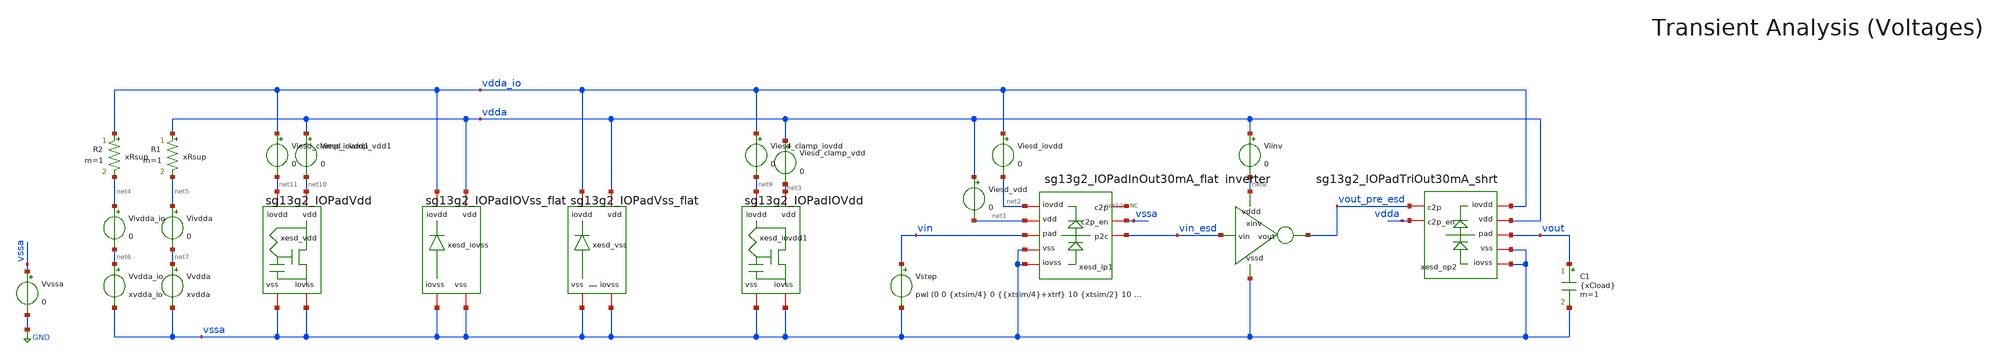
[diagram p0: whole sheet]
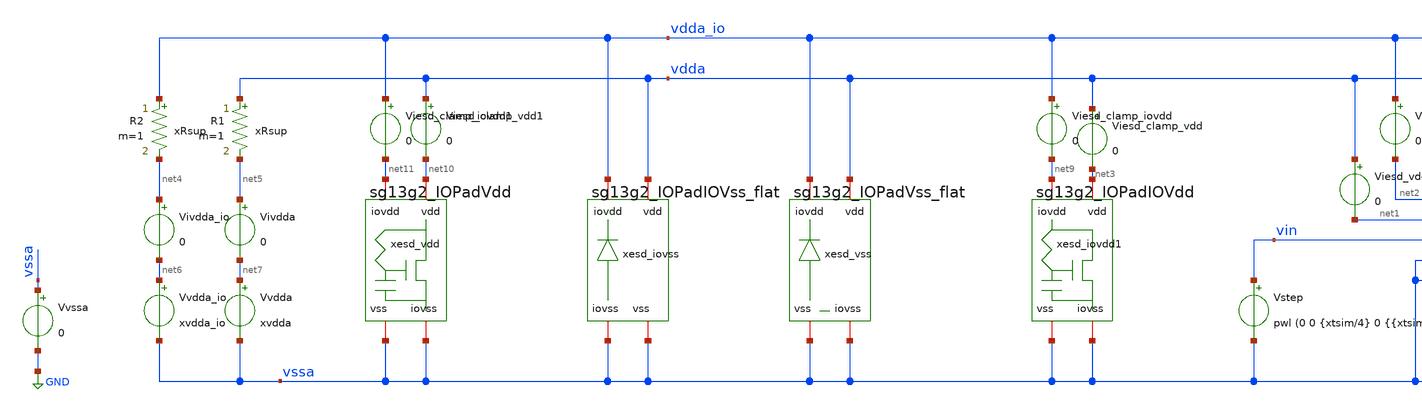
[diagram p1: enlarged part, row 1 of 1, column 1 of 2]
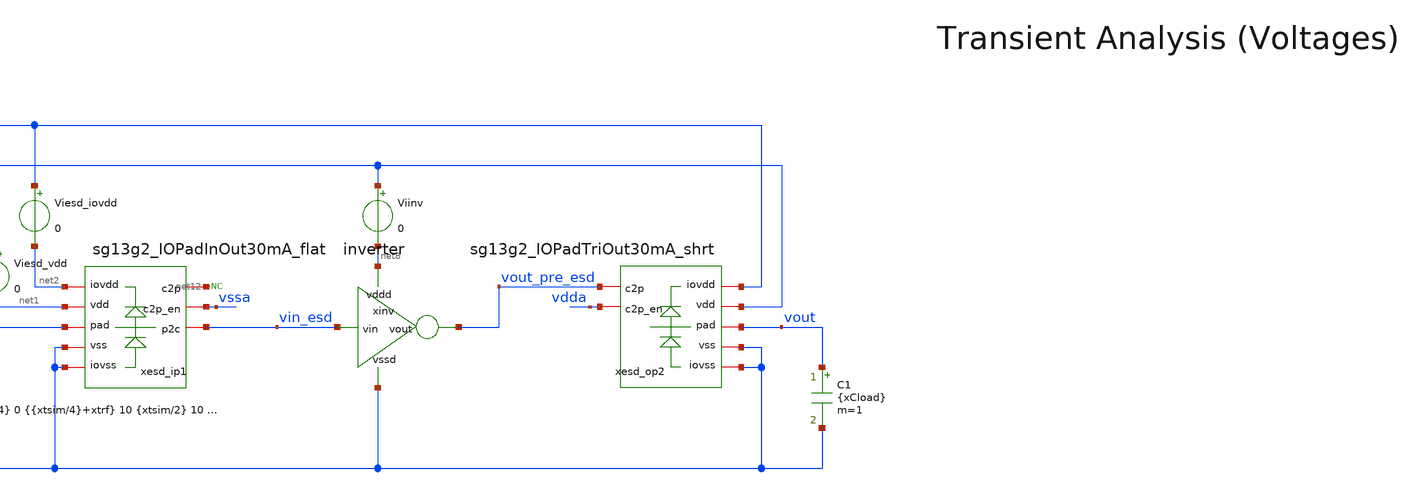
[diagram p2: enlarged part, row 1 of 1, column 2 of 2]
** sch_path: tb_inverter_demo/inverter_tb.sch
**.subckt inverter_tb
Vvssa vssa GND 0
Vvdda net7 vssa xvdda
Vstep vin vssa pwl (0 0 {xtsim/4} 0 {{xtsim/4}+xtrf} 10 {xtsim/2} 10 {{xtsim/2}+xtrf} 0)
xinv vin_esd vout_pre_esd net8 vssa inverter
Vvdda_io net6 vssa xvdda_io
* noconn #net12
C1 vout vssa {xCload} m=1
Viesd_clamp_vdd vdda net3 0
R1 vdda net5 xRsup m=1
R2 vdda_io net4 xRsup m=1
Vivdda_io net4 net6 0
Vivdda net5 net7 0
Viesd_iovdd vdda_io net2 0
Viesd_vdd vdda net1 0
Viinv vdda net8 0
Viesd_clamp_iovdd vdda_io net9 0
Viesd_clamp_vdd1 vdda net10 0
Viesd_clamp_iovdd1 vdda_io net11 0
xesd_ip1 vin_esd net2 vssa net1 vssa vin net12 vssa sg13g2_IOPadInOut30mA_flat
xesd_op2 vdda_io vssa vdda vssa vout_pre_esd vdda vout sg13g2_IOPadTriOut30mA_shrt
xesd_iovdd1 net9 vssa net3 vssa sg13g2_IOPadIOVdd
xesd_vdd net11 vssa net10 vssa sg13g2_IOPadVdd
xesd_vss vdda_io vssa vdda vssa sg13g2_IOPadVss_flat
xesd_iovss vdda_io vssa vdda vssa sg13g2_IOPadIOVss_flat
**** begin user architecture code

** opencircuitdesign pdks install
.lib /home/slice/pdk/iHP/IHP-Open-PDK/ihp-sg13g2/libs.tech/ngspice/models/cornerMOSlv.lib mos_tt
*.include /home/slice/xschem/tb_inverter/PEX/RC/output/inverter2__TOP/magic_RC/inverter.spice
.lib /home/slice/pdk/iHP/IHP-Open-PDK/ihp-sg13g2/libs.tech/ngspice/models/cornerMOShv.lib mos_tt
.lib /home/slice/pdk/iHP/IHP-Open-PDK/ihp-sg13g2/libs.tech/ngspice/models/cornerRES.lib res_typ
.include /home/slice/pdk/iHP/IHP-Open-PDK/ihp-sg13g2/libs.tech/ngspice/models/diodes.lib


* Parameters
.param xvdda = 1.5
.param xvdda_io = 3.3
.csparam xvdda_var = 'xvdda'
.param xCload = 50f
.param xtrf = 4.5n
.param xRsup = 1000
.param xtsim = 5u
.csparam xtsim_var = 'xtsim'

* vlogA instantiation
.model OTA_vcvs OTA_vcvs

  ** must save the below for DCOP analysis to be back annotated onto the schematic
  .option savecurrents
  .save

  +  @n.xinv.xM_NMOS.nsg13_lv_nmos[vgs]
  +  @n.xinv.xM_NMOS.nsg13_lv_nmos[vds]
  +  @n.xinv.xM_NMOS.nsg13_lv_nmos[vth]
  +  @n.xinv.xM_NMOS.nsg13_lv_nmos[gds]
  +  @n.xinv.xM_NMOS.nsg13_lv_nmos[gm]
  +  @n.xinv.xM_NMOS.nsg13_lv_nmos[ids]
  +  @n.xinv.xM_NMOS.nsg13_lv_nmos[vsat]

  +  @n.xinv.xM_PMOS.nsg13_lv_pmos[vgs]
  +  @n.xinv.xM_PMOS.nsg13_lv_pmos[vds]
  +  @n.xinv.xM_PMOS.nsg13_lv_pmos[vth]
  +  @n.xinv.xM_PMOS.nsg13_lv_pmos[gds]
  +  @n.xinv.xM_PMOS.nsg13_lv_pmos[gm]
  +  @n.xinv.xM_PMOS.nsg13_lv_pmos[ids]
  +  @n.xinv.xM_PMOS.nsg13_lv_pmos[vsat]


  .save v(vout) v(vin) v(vdda) v(vssa) v(vout_sch) v(vout_rcpex) v(vin_esd) v(vout_pre_esd)
  .save i(xinv.vdda) i(v.xota.Vitail)

  .control
  pre_osdi OTA_vcvs.osdi
  save all

** 1. DCOP ANALYSIS **

  op
 * set filetype=ascii
  remzerovec
  write tb_inv_op.raw

** 2. TRAN ANALYSIS **

  tran 1n $&xtsim_var
  remzerovec
  write tb_inv_tran.raw

** 3. MEASURES **

  echo --
  meas TRAN t_90_10 TRIG v(vout) VAL=0.9*xvdda_var FALL=1 TARG v(vout) VAL=0.1*xvdda_var FALL=1
  meas TRAN t_10_90 TRIG v(vout) VAL=0.1*xvdda_var RISE=1 TARG v(vout) VAL=0.9*xvdda_var RISE=1
  echo --

  setplot
*quit 0
.endc




**** end user architecture code
**.ends
.GLOBAL GND
.end
